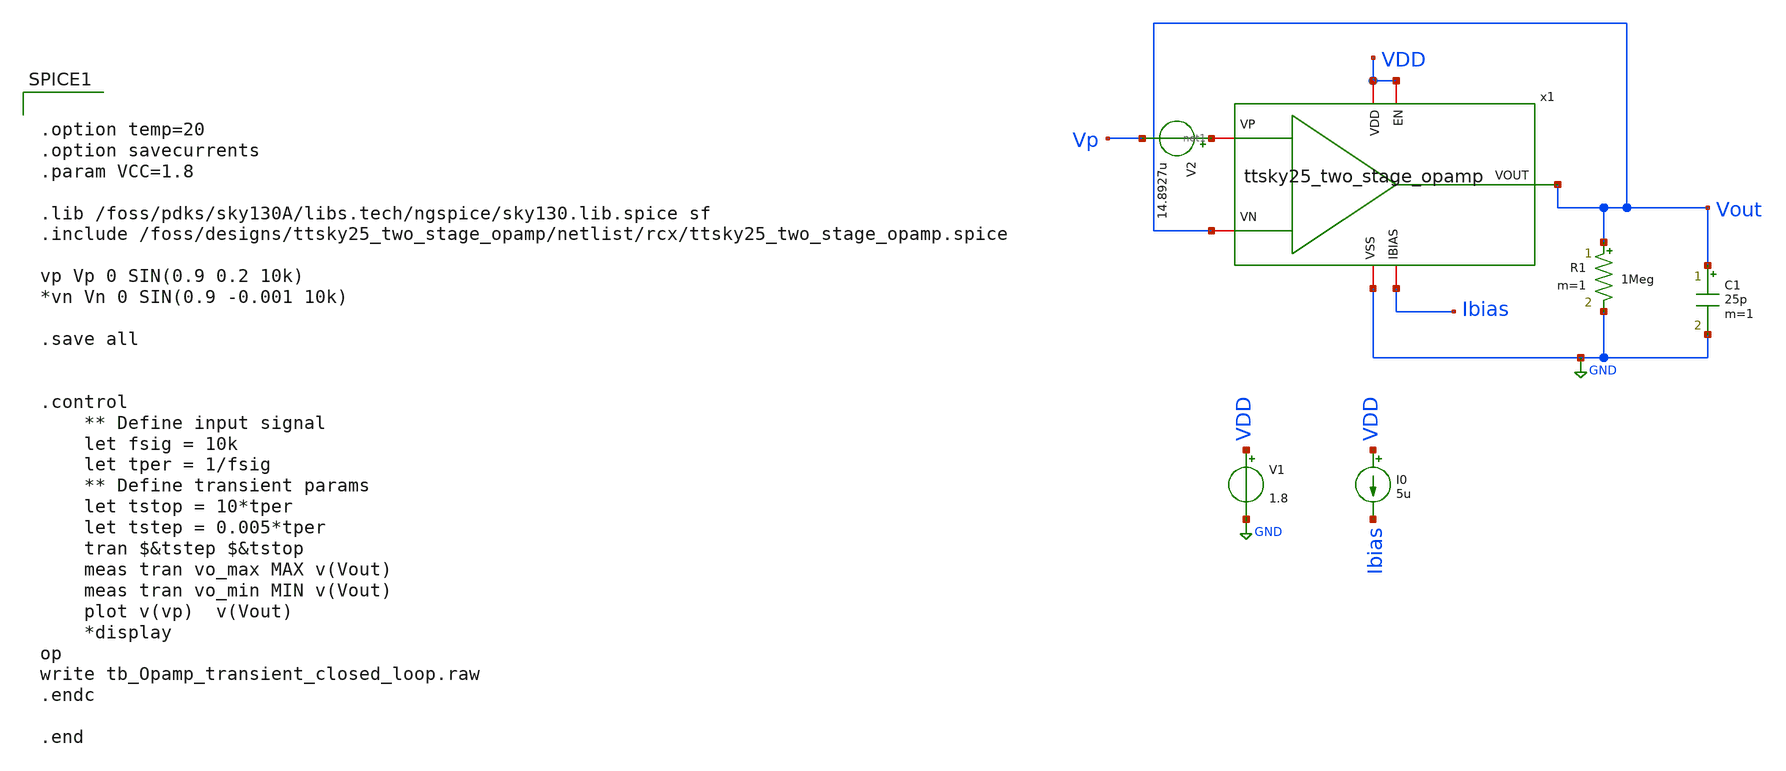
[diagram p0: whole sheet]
** sch_path: xschem/post-layout/testbenches/tb_Opamp_transient_closed_loop.sch
**.subckt tb_Opamp_transient_closed_loop
V1 VDD GND 1.8
I0 VDD Ibias 5u
C1 Vout GND 25p m=1
x1 VDD Ibias Vout Vout net1 VDD GND ttsky25_two_stage_opamp
V2 net1 Vp 14.8927u
R1 Vout GND 1Meg m=1
**** begin user architecture code


.option temp=20
.option savecurrents
.param VCC=1.8

.lib /foss/pdks/sky130A/libs.tech/ngspice/sky130.lib.spice sf
.include /foss/designs/ttsky25_two_stage_opamp/netlist/rcx/ttsky25_two_stage_opamp.spice

vp Vp 0 SIN(0.9 0.2 10k)
*vn Vn 0 SIN(0.9 -0.001 10k)

.save all


.control
	** Define input signal
	let fsig = 10k
	let tper = 1/fsig
	** Define transient params
	let tstop = 10*tper
	let tstep = 0.005*tper
	tran $&tstep $&tstop
	meas tran vo_max MAX v(Vout)
	meas tran vo_min MIN v(Vout)
	plot v(vp)  v(Vout)
	*display
op
write tb_Opamp_transient_closed_loop.raw
.endc

.end


**** end user architecture code
**.ends
.GLOBAL GND
.end
